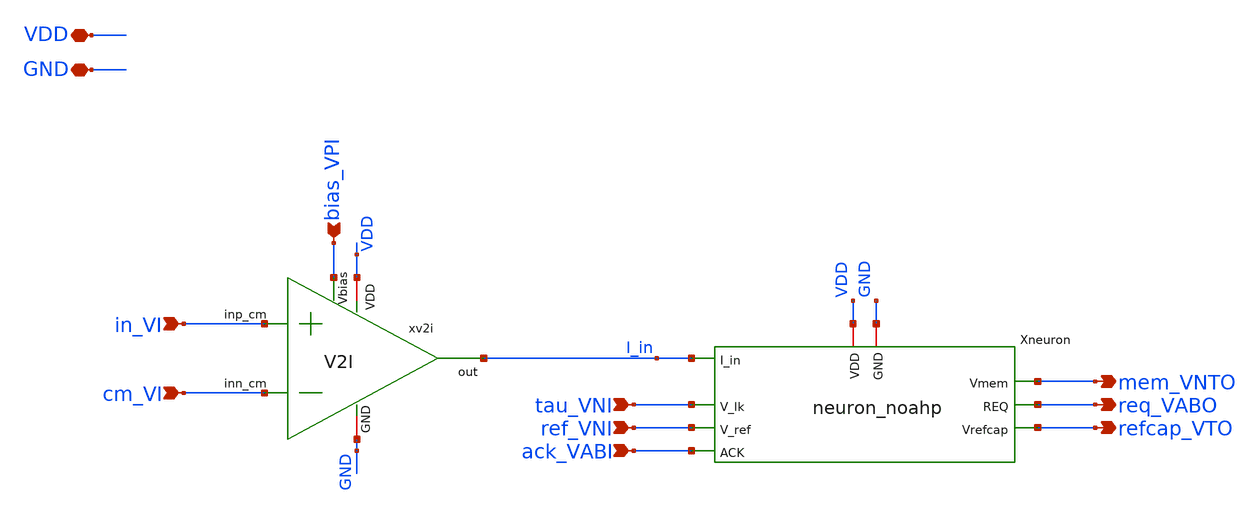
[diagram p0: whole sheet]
** sch_path: xschem/neuron_row.sch
**.subckt neuron_row in_VI cm_VI bias_VPI VDD GND mem_VNTO req_VABO refcap_VTO tau_VNI ref_VNI
*+ ack_VABI
*.ipin in_VI
*.ipin cm_VI
*.ipin bias_VPI
*.iopin VDD
*.iopin GND
*.opin mem_VNTO
*.opin req_VABO
*.opin refcap_VTO
*.ipin tau_VNI
*.ipin ref_VNI
*.ipin ack_VABI
Xneuron VDD I_in tau_VNI mem_VNTO req_VABO ack_VABI ref_VNI GND refcap_VTO neuron_noahp
xv2i VDD bias_VPI cm_VI in_VI I_in GND V2I
**.ends
.end
